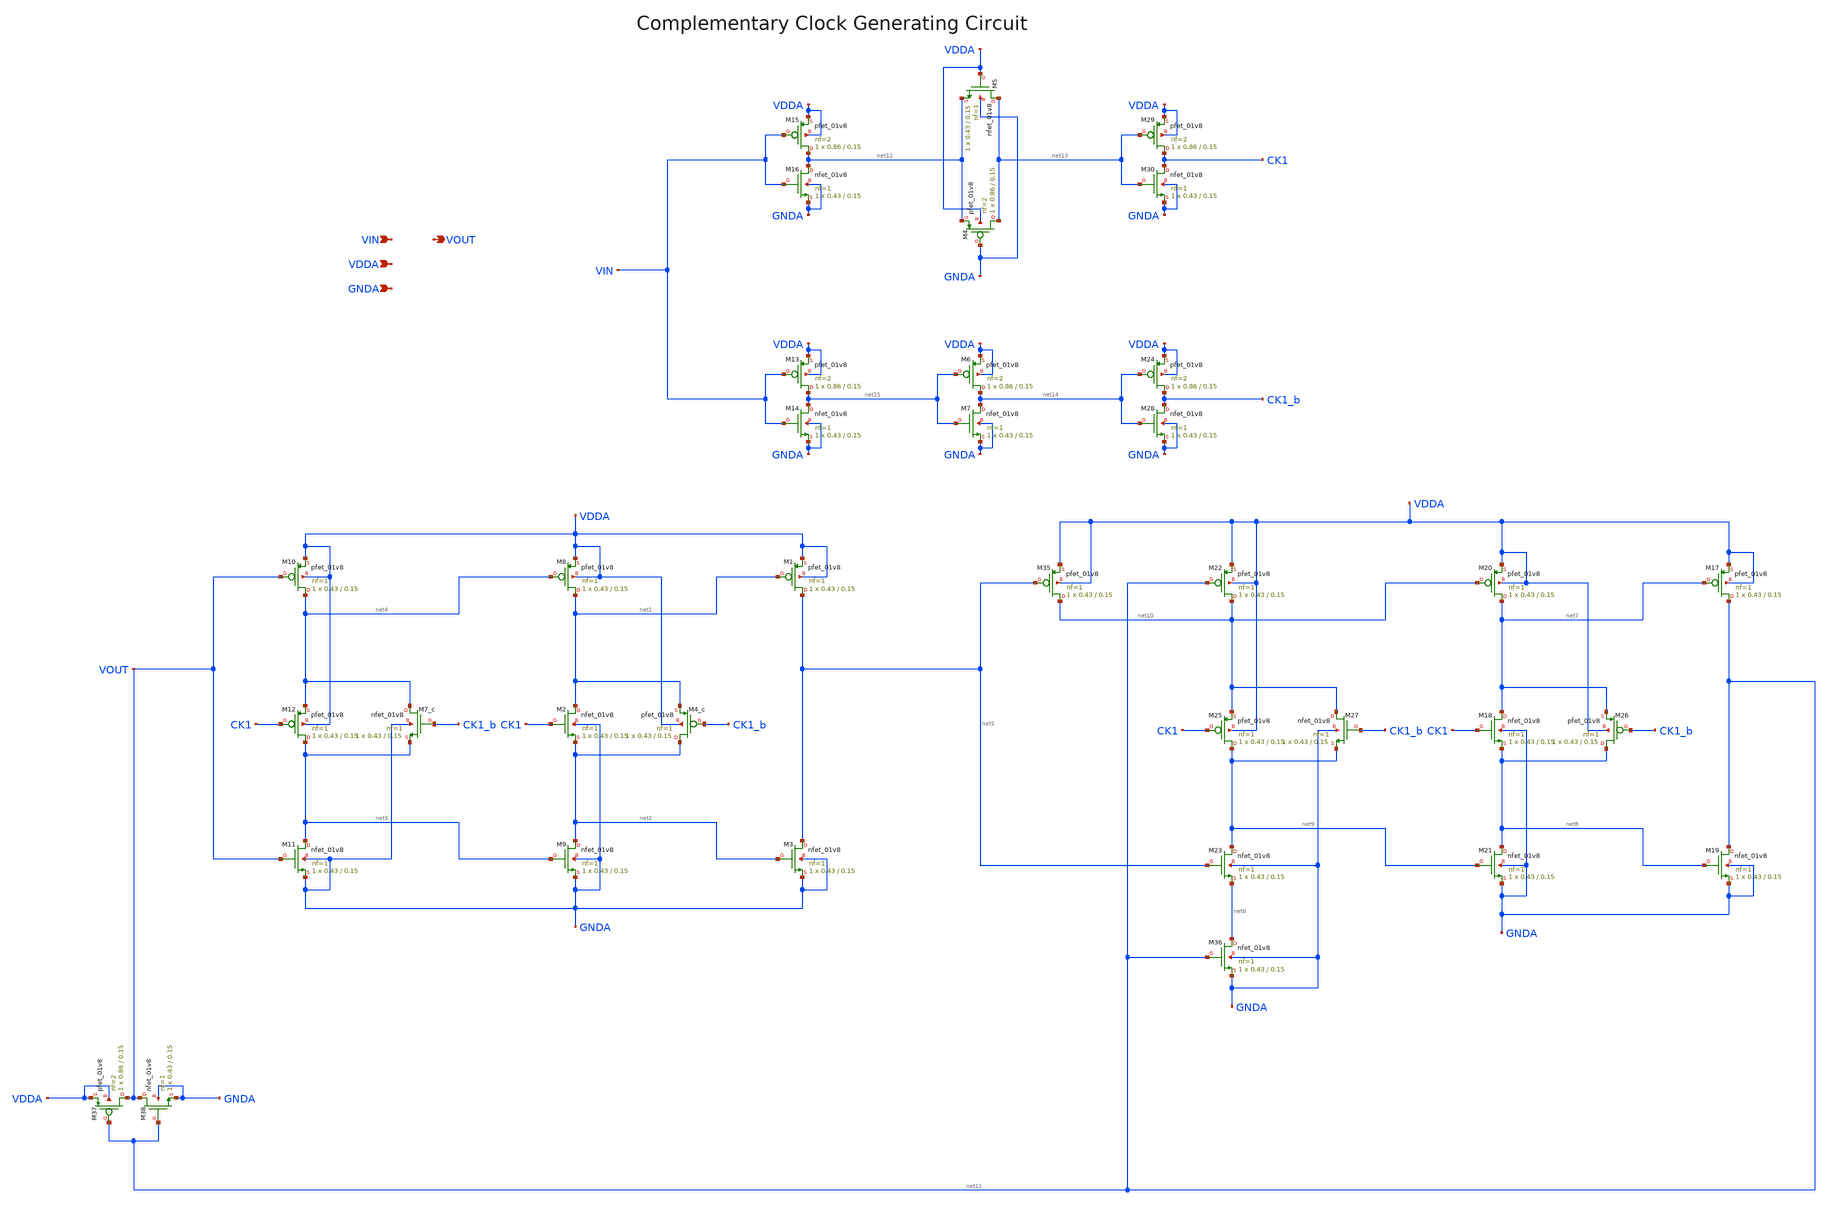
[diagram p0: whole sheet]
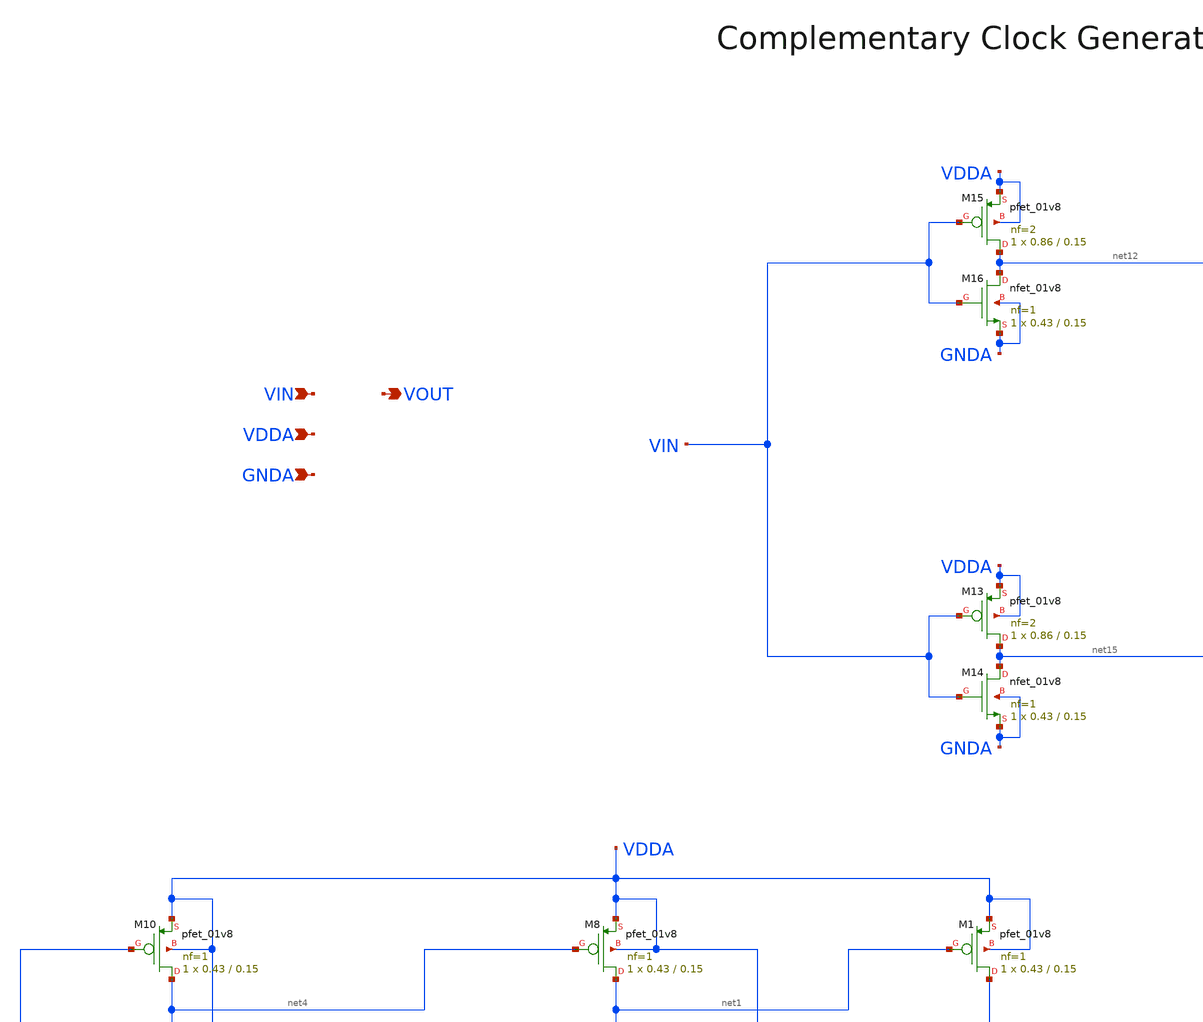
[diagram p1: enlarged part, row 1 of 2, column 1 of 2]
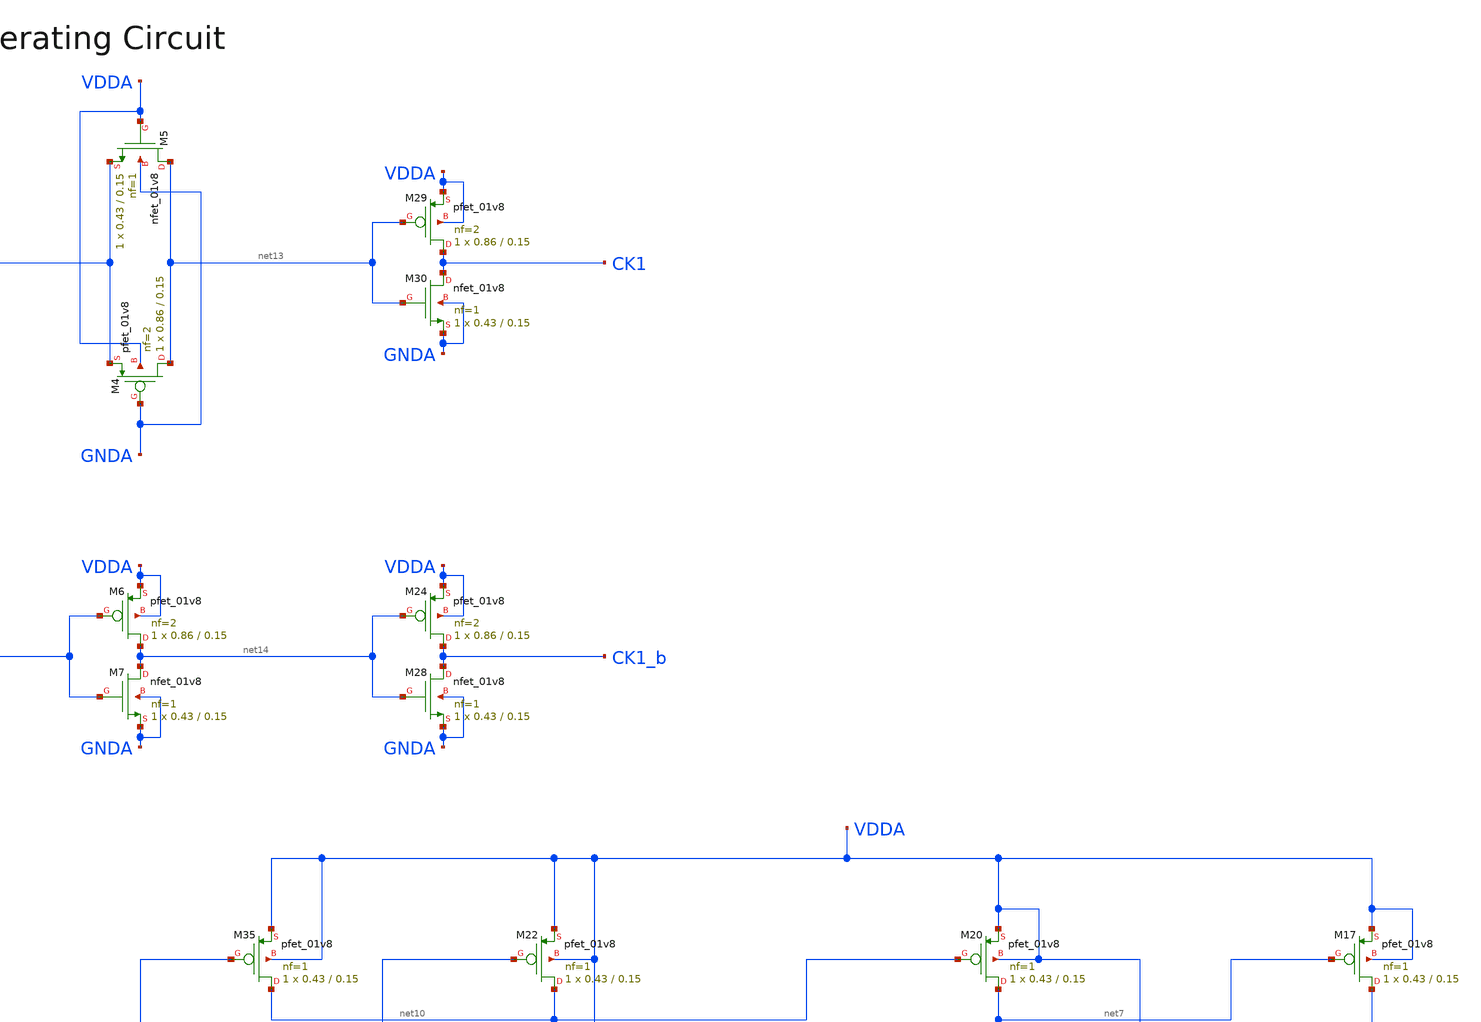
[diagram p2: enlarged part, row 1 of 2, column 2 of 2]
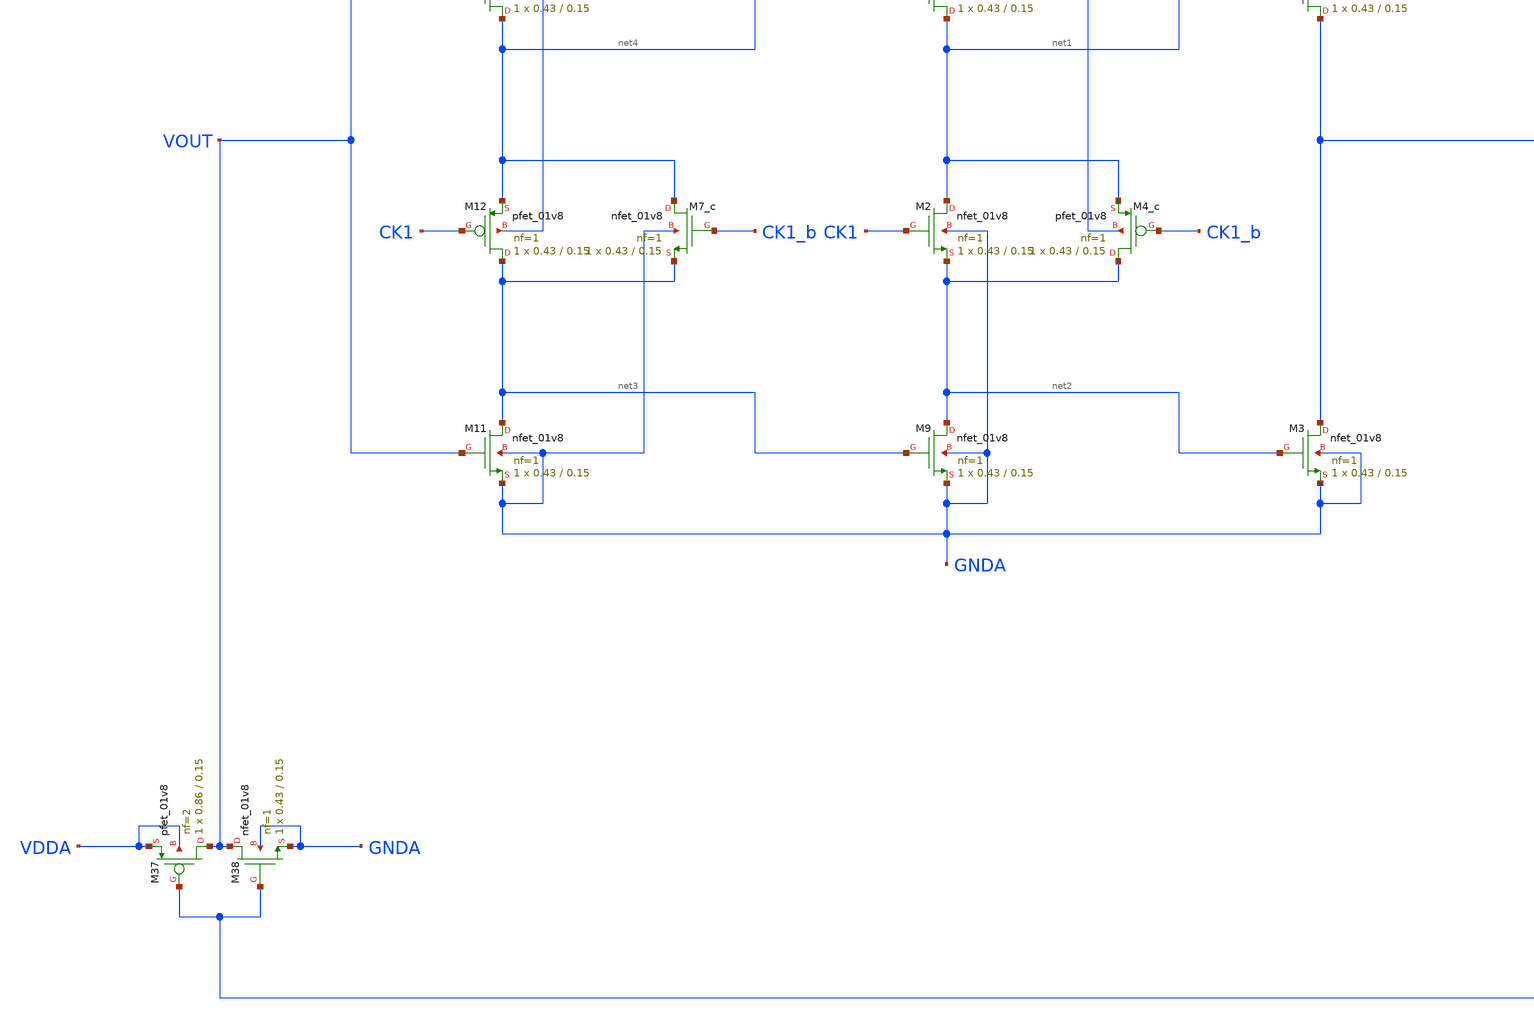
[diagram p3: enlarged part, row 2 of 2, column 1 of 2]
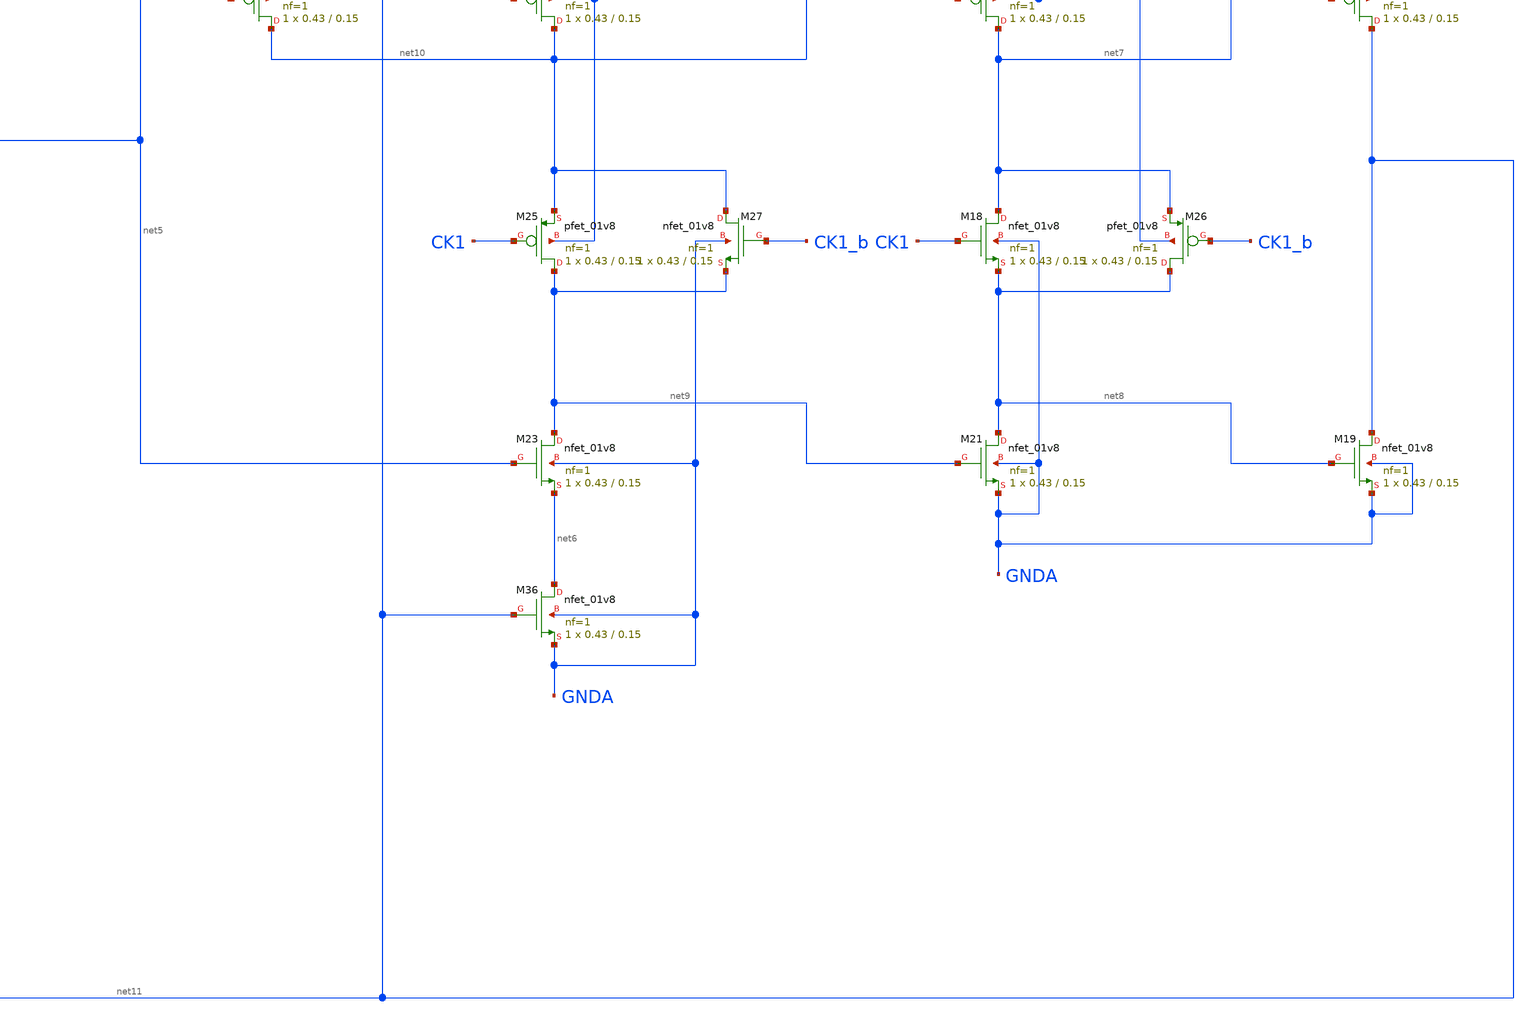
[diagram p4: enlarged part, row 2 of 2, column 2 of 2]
** sch_path: projects/pll/divider/xschem_ngspice/FF_comp_sw_divide3_2.sch
**.subckt FF_comp_sw_divide3_2 VIN VOUT VDDA GNDA
*.ipin VIN
*.opin VOUT
*.ipin VDDA
*.ipin GNDA
XM1 net5 net1 VDDA VDDA sky130_fd_pr__pfet_01v8 L=0.15 W=0.43 nf=1 ad='int((nf+1)/2) * W/nf * 0.29' as='int((nf+2)/2) * W/nf * 0.29'
+ pd='2*int((nf+1)/2) * (W/nf + 0.29)' ps='2*int((nf+2)/2) * (W/nf + 0.29)' nrd='0.29 / W' nrs='0.29 / W'
+ sa=0 sb=0 sd=0 mult=1 m=1
XM2 net1 CK1 net2 GNDA sky130_fd_pr__nfet_01v8 L=0.15 W=0.43 nf=1 ad='int((nf+1)/2) * W/nf * 0.29' as='int((nf+2)/2) * W/nf * 0.29'
+ pd='2*int((nf+1)/2) * (W/nf + 0.29)' ps='2*int((nf+2)/2) * (W/nf + 0.29)' nrd='0.29 / W' nrs='0.29 / W'
+ sa=0 sb=0 sd=0 mult=1 m=1
XM3 net5 net2 GNDA GNDA sky130_fd_pr__nfet_01v8 L=0.15 W=0.43 nf=1 ad='int((nf+1)/2) * W/nf * 0.29' as='int((nf+2)/2) * W/nf * 0.29'
+ pd='2*int((nf+1)/2) * (W/nf + 0.29)' ps='2*int((nf+2)/2) * (W/nf + 0.29)' nrd='0.29 / W' nrs='0.29 / W'
+ sa=0 sb=0 sd=0 mult=1 m=1
XM8 net1 net4 VDDA VDDA sky130_fd_pr__pfet_01v8 L=0.15 W=0.43 nf=1 ad='int((nf+1)/2) * W/nf * 0.29' as='int((nf+2)/2) * W/nf * 0.29'
+ pd='2*int((nf+1)/2) * (W/nf + 0.29)' ps='2*int((nf+2)/2) * (W/nf + 0.29)' nrd='0.29 / W' nrs='0.29 / W'
+ sa=0 sb=0 sd=0 mult=1 m=1
XM9 net2 net3 GNDA GNDA sky130_fd_pr__nfet_01v8 L=0.15 W=0.43 nf=1 ad='int((nf+1)/2) * W/nf * 0.29' as='int((nf+2)/2) * W/nf * 0.29'
+ pd='2*int((nf+1)/2) * (W/nf + 0.29)' ps='2*int((nf+2)/2) * (W/nf + 0.29)' nrd='0.29 / W' nrs='0.29 / W'
+ sa=0 sb=0 sd=0 mult=1 m=1
XM10 net4 VOUT VDDA VDDA sky130_fd_pr__pfet_01v8 L=0.15 W=0.43 nf=1 ad='int((nf+1)/2) * W/nf * 0.29'
+ as='int((nf+2)/2) * W/nf * 0.29' pd='2*int((nf+1)/2) * (W/nf + 0.29)' ps='2*int((nf+2)/2) * (W/nf + 0.29)'
+ nrd='0.29 / W' nrs='0.29 / W' sa=0 sb=0 sd=0 mult=1 m=1
XM11 net3 VOUT GNDA GNDA sky130_fd_pr__nfet_01v8 L=0.15 W=0.43 nf=1 ad='int((nf+1)/2) * W/nf * 0.29'
+ as='int((nf+2)/2) * W/nf * 0.29' pd='2*int((nf+1)/2) * (W/nf + 0.29)' ps='2*int((nf+2)/2) * (W/nf + 0.29)'
+ nrd='0.29 / W' nrs='0.29 / W' sa=0 sb=0 sd=0 mult=1 m=1
XM12 net3 CK1 net4 VDDA sky130_fd_pr__pfet_01v8 L=0.15 W=0.43 nf=1 ad='int((nf+1)/2) * W/nf * 0.29' as='int((nf+2)/2) * W/nf * 0.29'
+ pd='2*int((nf+1)/2) * (W/nf + 0.29)' ps='2*int((nf+2)/2) * (W/nf + 0.29)' nrd='0.29 / W' nrs='0.29 / W'
+ sa=0 sb=0 sd=0 mult=1 m=1
XM4_c net2 CK1_b net1 VDDA sky130_fd_pr__pfet_01v8 L=0.15 W=0.43 nf=1 ad='int((nf+1)/2) * W/nf * 0.29'
+ as='int((nf+2)/2) * W/nf * 0.29' pd='2*int((nf+1)/2) * (W/nf + 0.29)' ps='2*int((nf+2)/2) * (W/nf + 0.29)'
+ nrd='0.29 / W' nrs='0.29 / W' sa=0 sb=0 sd=0 mult=1 m=1
XM7_c net4 CK1_b net3 GNDA sky130_fd_pr__nfet_01v8 L=0.15 W=0.43 nf=1 ad='int((nf+1)/2) * W/nf * 0.29'
+ as='int((nf+2)/2) * W/nf * 0.29' pd='2*int((nf+1)/2) * (W/nf + 0.29)' ps='2*int((nf+2)/2) * (W/nf + 0.29)'
+ nrd='0.29 / W' nrs='0.29 / W' sa=0 sb=0 sd=0 mult=1 m=1
XM17 net11 net7 VDDA VDDA sky130_fd_pr__pfet_01v8 L=0.15 W=0.43 nf=1 ad='int((nf+1)/2) * W/nf * 0.29'
+ as='int((nf+2)/2) * W/nf * 0.29' pd='2*int((nf+1)/2) * (W/nf + 0.29)' ps='2*int((nf+2)/2) * (W/nf + 0.29)'
+ nrd='0.29 / W' nrs='0.29 / W' sa=0 sb=0 sd=0 mult=1 m=1
XM18 net7 CK1 net8 GNDA sky130_fd_pr__nfet_01v8 L=0.15 W=0.43 nf=1 ad='int((nf+1)/2) * W/nf * 0.29' as='int((nf+2)/2) * W/nf * 0.29'
+ pd='2*int((nf+1)/2) * (W/nf + 0.29)' ps='2*int((nf+2)/2) * (W/nf + 0.29)' nrd='0.29 / W' nrs='0.29 / W'
+ sa=0 sb=0 sd=0 mult=1 m=1
XM19 net11 net8 GNDA GNDA sky130_fd_pr__nfet_01v8 L=0.15 W=0.43 nf=1 ad='int((nf+1)/2) * W/nf * 0.29'
+ as='int((nf+2)/2) * W/nf * 0.29' pd='2*int((nf+1)/2) * (W/nf + 0.29)' ps='2*int((nf+2)/2) * (W/nf + 0.29)'
+ nrd='0.29 / W' nrs='0.29 / W' sa=0 sb=0 sd=0 mult=1 m=1
XM20 net7 net10 VDDA VDDA sky130_fd_pr__pfet_01v8 L=0.15 W=0.43 nf=1 ad='int((nf+1)/2) * W/nf * 0.29'
+ as='int((nf+2)/2) * W/nf * 0.29' pd='2*int((nf+1)/2) * (W/nf + 0.29)' ps='2*int((nf+2)/2) * (W/nf + 0.29)'
+ nrd='0.29 / W' nrs='0.29 / W' sa=0 sb=0 sd=0 mult=1 m=1
XM21 net8 net9 GNDA GNDA sky130_fd_pr__nfet_01v8 L=0.15 W=0.43 nf=1 ad='int((nf+1)/2) * W/nf * 0.29'
+ as='int((nf+2)/2) * W/nf * 0.29' pd='2*int((nf+1)/2) * (W/nf + 0.29)' ps='2*int((nf+2)/2) * (W/nf + 0.29)'
+ nrd='0.29 / W' nrs='0.29 / W' sa=0 sb=0 sd=0 mult=1 m=1
XM22 net10 net11 VDDA VDDA sky130_fd_pr__pfet_01v8 L=0.15 W=0.43 nf=1 ad='int((nf+1)/2) * W/nf * 0.29'
+ as='int((nf+2)/2) * W/nf * 0.29' pd='2*int((nf+1)/2) * (W/nf + 0.29)' ps='2*int((nf+2)/2) * (W/nf + 0.29)'
+ nrd='0.29 / W' nrs='0.29 / W' sa=0 sb=0 sd=0 mult=1 m=1
XM23 net9 net5 net6 GNDA sky130_fd_pr__nfet_01v8 L=0.15 W=0.43 nf=1 ad='int((nf+1)/2) * W/nf * 0.29'
+ as='int((nf+2)/2) * W/nf * 0.29' pd='2*int((nf+1)/2) * (W/nf + 0.29)' ps='2*int((nf+2)/2) * (W/nf + 0.29)'
+ nrd='0.29 / W' nrs='0.29 / W' sa=0 sb=0 sd=0 mult=1 m=1
XM25 net9 CK1 net10 VDDA sky130_fd_pr__pfet_01v8 L=0.15 W=0.43 nf=1 ad='int((nf+1)/2) * W/nf * 0.29'
+ as='int((nf+2)/2) * W/nf * 0.29' pd='2*int((nf+1)/2) * (W/nf + 0.29)' ps='2*int((nf+2)/2) * (W/nf + 0.29)'
+ nrd='0.29 / W' nrs='0.29 / W' sa=0 sb=0 sd=0 mult=1 m=1
XM26 net8 CK1_b net7 VDDA sky130_fd_pr__pfet_01v8 L=0.15 W=0.43 nf=1 ad='int((nf+1)/2) * W/nf * 0.29'
+ as='int((nf+2)/2) * W/nf * 0.29' pd='2*int((nf+1)/2) * (W/nf + 0.29)' ps='2*int((nf+2)/2) * (W/nf + 0.29)'
+ nrd='0.29 / W' nrs='0.29 / W' sa=0 sb=0 sd=0 mult=1 m=1
XM27 net10 CK1_b net9 GNDA sky130_fd_pr__nfet_01v8 L=0.15 W=0.43 nf=1 ad='int((nf+1)/2) * W/nf * 0.29'
+ as='int((nf+2)/2) * W/nf * 0.29' pd='2*int((nf+1)/2) * (W/nf + 0.29)' ps='2*int((nf+2)/2) * (W/nf + 0.29)'
+ nrd='0.29 / W' nrs='0.29 / W' sa=0 sb=0 sd=0 mult=1 m=1
XM35 net10 net5 VDDA VDDA sky130_fd_pr__pfet_01v8 L=0.15 W=0.43 nf=1 ad='int((nf+1)/2) * W/nf * 0.29'
+ as='int((nf+2)/2) * W/nf * 0.29' pd='2*int((nf+1)/2) * (W/nf + 0.29)' ps='2*int((nf+2)/2) * (W/nf + 0.29)'
+ nrd='0.29 / W' nrs='0.29 / W' sa=0 sb=0 sd=0 mult=1 m=1
XM36 net6 net11 GNDA GNDA sky130_fd_pr__nfet_01v8 L=0.15 W=0.43 nf=1 ad='int((nf+1)/2) * W/nf * 0.29'
+ as='int((nf+2)/2) * W/nf * 0.29' pd='2*int((nf+1)/2) * (W/nf + 0.29)' ps='2*int((nf+2)/2) * (W/nf + 0.29)'
+ nrd='0.29 / W' nrs='0.29 / W' sa=0 sb=0 sd=0 mult=1 m=1
XM37 VOUT net11 VDDA VDDA sky130_fd_pr__pfet_01v8 L=0.15 W=0.86 nf=2 ad='int((nf+1)/2) * W/nf * 0.29'
+ as='int((nf+2)/2) * W/nf * 0.29' pd='2*int((nf+1)/2) * (W/nf + 0.29)' ps='2*int((nf+2)/2) * (W/nf + 0.29)'
+ nrd='0.29 / W' nrs='0.29 / W' sa=0 sb=0 sd=0 mult=1 m=1
XM38 VOUT net11 GNDA GNDA sky130_fd_pr__nfet_01v8 L=0.15 W=0.43 nf=1 ad='int((nf+1)/2) * W/nf * 0.29'
+ as='int((nf+2)/2) * W/nf * 0.29' pd='2*int((nf+1)/2) * (W/nf + 0.29)' ps='2*int((nf+2)/2) * (W/nf + 0.29)'
+ nrd='0.29 / W' nrs='0.29 / W' sa=0 sb=0 sd=0 mult=1 m=1
XM4 net13 GNDA net12 VDDA sky130_fd_pr__pfet_01v8 L=0.15 W=0.86 nf=2 ad='int((nf+1)/2) * W/nf * 0.29'
+ as='int((nf+2)/2) * W/nf * 0.29' pd='2*int((nf+1)/2) * (W/nf + 0.29)' ps='2*int((nf+2)/2) * (W/nf + 0.29)'
+ nrd='0.29 / W' nrs='0.29 / W' sa=0 sb=0 sd=0 mult=1 m=1
XM5 net13 VDDA net12 GNDA sky130_fd_pr__nfet_01v8 L=0.15 W=0.43 nf=1 ad='int((nf+1)/2) * W/nf * 0.29'
+ as='int((nf+2)/2) * W/nf * 0.29' pd='2*int((nf+1)/2) * (W/nf + 0.29)' ps='2*int((nf+2)/2) * (W/nf + 0.29)'
+ nrd='0.29 / W' nrs='0.29 / W' sa=0 sb=0 sd=0 mult=1 m=1
XM6 net14 net15 VDDA VDDA sky130_fd_pr__pfet_01v8 L=0.15 W=0.86 nf=2 ad='int((nf+1)/2) * W/nf * 0.29'
+ as='int((nf+2)/2) * W/nf * 0.29' pd='2*int((nf+1)/2) * (W/nf + 0.29)' ps='2*int((nf+2)/2) * (W/nf + 0.29)'
+ nrd='0.29 / W' nrs='0.29 / W' sa=0 sb=0 sd=0 mult=1 m=1
XM7 net14 net15 GNDA GNDA sky130_fd_pr__nfet_01v8 L=0.15 W=0.43 nf=1 ad='int((nf+1)/2) * W/nf * 0.29'
+ as='int((nf+2)/2) * W/nf * 0.29' pd='2*int((nf+1)/2) * (W/nf + 0.29)' ps='2*int((nf+2)/2) * (W/nf + 0.29)'
+ nrd='0.29 / W' nrs='0.29 / W' sa=0 sb=0 sd=0 mult=1 m=1
XM13 net15 VIN VDDA VDDA sky130_fd_pr__pfet_01v8 L=0.15 W=0.86 nf=2 ad='int((nf+1)/2) * W/nf * 0.29'
+ as='int((nf+2)/2) * W/nf * 0.29' pd='2*int((nf+1)/2) * (W/nf + 0.29)' ps='2*int((nf+2)/2) * (W/nf + 0.29)'
+ nrd='0.29 / W' nrs='0.29 / W' sa=0 sb=0 sd=0 mult=1 m=1
XM14 net15 VIN GNDA GNDA sky130_fd_pr__nfet_01v8 L=0.15 W=0.43 nf=1 ad='int((nf+1)/2) * W/nf * 0.29'
+ as='int((nf+2)/2) * W/nf * 0.29' pd='2*int((nf+1)/2) * (W/nf + 0.29)' ps='2*int((nf+2)/2) * (W/nf + 0.29)'
+ nrd='0.29 / W' nrs='0.29 / W' sa=0 sb=0 sd=0 mult=1 m=1
XM15 net12 VIN VDDA VDDA sky130_fd_pr__pfet_01v8 L=0.15 W=0.86 nf=2 ad='int((nf+1)/2) * W/nf * 0.29'
+ as='int((nf+2)/2) * W/nf * 0.29' pd='2*int((nf+1)/2) * (W/nf + 0.29)' ps='2*int((nf+2)/2) * (W/nf + 0.29)'
+ nrd='0.29 / W' nrs='0.29 / W' sa=0 sb=0 sd=0 mult=1 m=1
XM16 net12 VIN GNDA GNDA sky130_fd_pr__nfet_01v8 L=0.15 W=0.43 nf=1 ad='int((nf+1)/2) * W/nf * 0.29'
+ as='int((nf+2)/2) * W/nf * 0.29' pd='2*int((nf+1)/2) * (W/nf + 0.29)' ps='2*int((nf+2)/2) * (W/nf + 0.29)'
+ nrd='0.29 / W' nrs='0.29 / W' sa=0 sb=0 sd=0 mult=1 m=1
XM24 CK1_b net14 VDDA VDDA sky130_fd_pr__pfet_01v8 L=0.15 W=0.86 nf=2 ad='int((nf+1)/2) * W/nf * 0.29'
+ as='int((nf+2)/2) * W/nf * 0.29' pd='2*int((nf+1)/2) * (W/nf + 0.29)' ps='2*int((nf+2)/2) * (W/nf + 0.29)'
+ nrd='0.29 / W' nrs='0.29 / W' sa=0 sb=0 sd=0 mult=1 m=1
XM28 CK1_b net14 GNDA GNDA sky130_fd_pr__nfet_01v8 L=0.15 W=0.43 nf=1 ad='int((nf+1)/2) * W/nf * 0.29'
+ as='int((nf+2)/2) * W/nf * 0.29' pd='2*int((nf+1)/2) * (W/nf + 0.29)' ps='2*int((nf+2)/2) * (W/nf + 0.29)'
+ nrd='0.29 / W' nrs='0.29 / W' sa=0 sb=0 sd=0 mult=1 m=1
XM29 CK1 net13 VDDA VDDA sky130_fd_pr__pfet_01v8 L=0.15 W=0.86 nf=2 ad='int((nf+1)/2) * W/nf * 0.29'
+ as='int((nf+2)/2) * W/nf * 0.29' pd='2*int((nf+1)/2) * (W/nf + 0.29)' ps='2*int((nf+2)/2) * (W/nf + 0.29)'
+ nrd='0.29 / W' nrs='0.29 / W' sa=0 sb=0 sd=0 mult=1 m=1
XM30 CK1 net13 GNDA GNDA sky130_fd_pr__nfet_01v8 L=0.15 W=0.43 nf=1 ad='int((nf+1)/2) * W/nf * 0.29'
+ as='int((nf+2)/2) * W/nf * 0.29' pd='2*int((nf+1)/2) * (W/nf + 0.29)' ps='2*int((nf+2)/2) * (W/nf + 0.29)'
+ nrd='0.29 / W' nrs='0.29 / W' sa=0 sb=0 sd=0 mult=1 m=1
**.ends
.end
